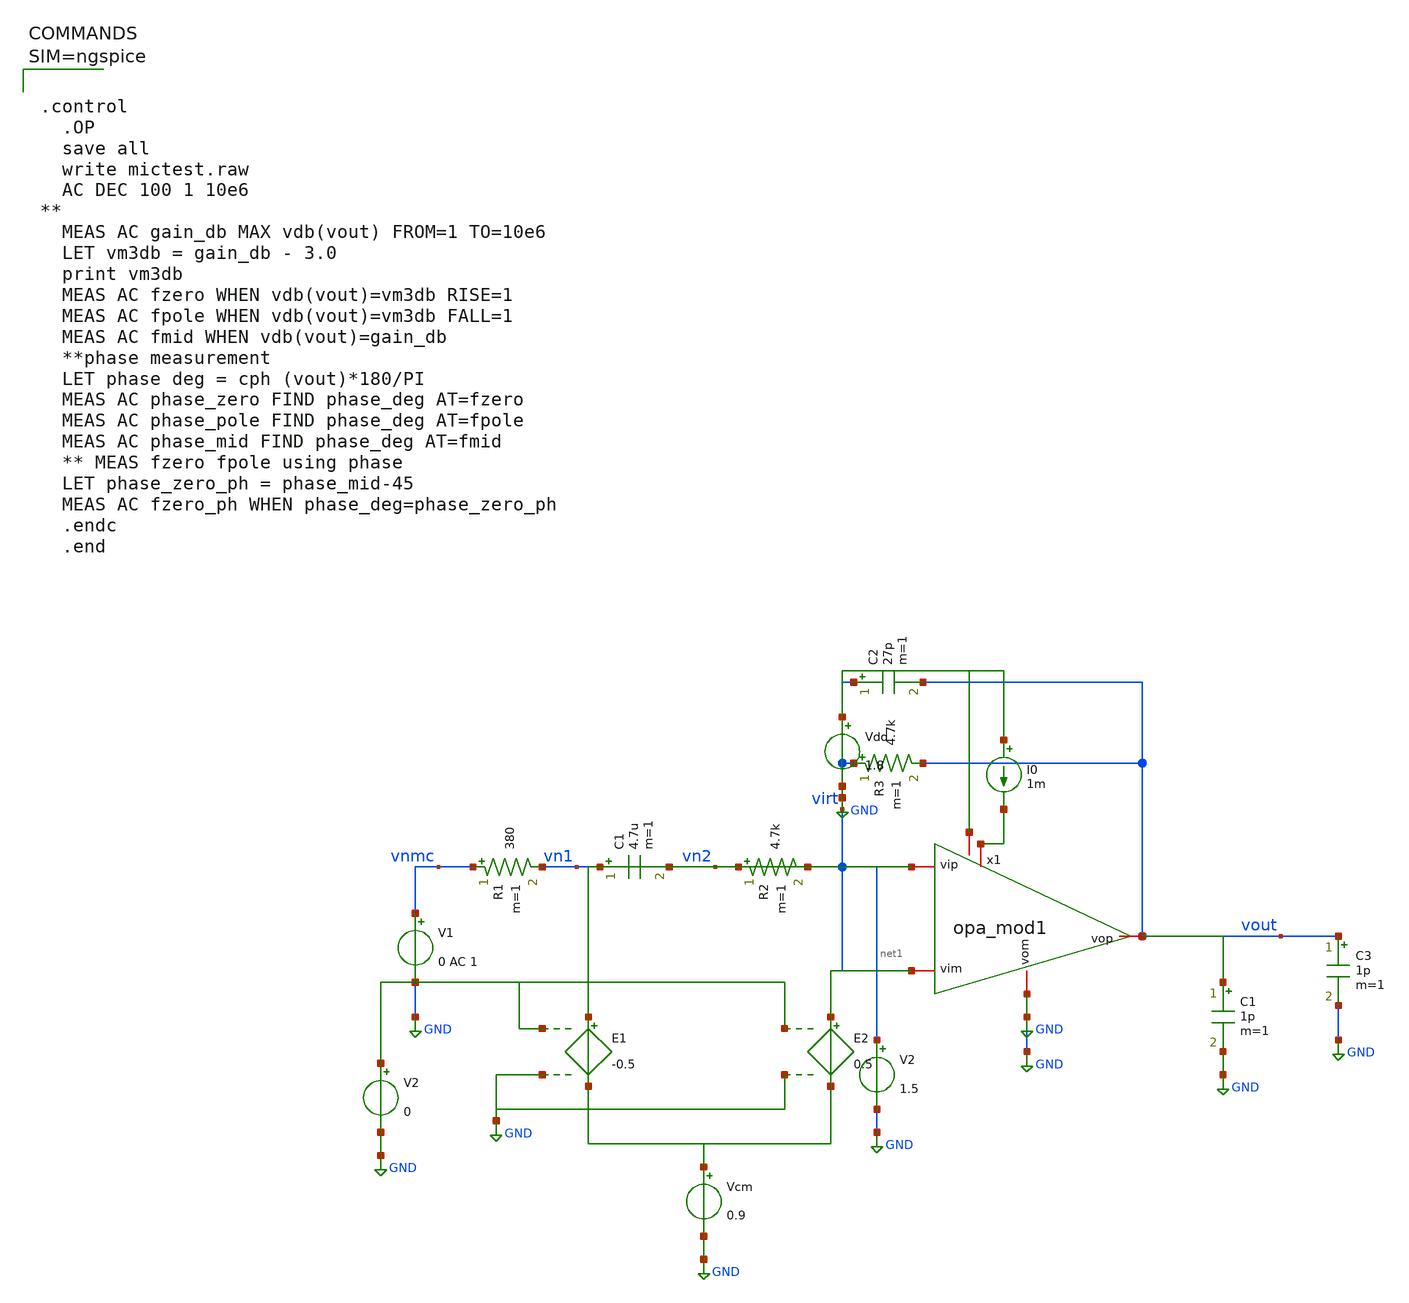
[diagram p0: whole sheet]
** sch_path: xschem/micTest_opamod1.sch
**.subckt micTest_opamod1
V1 vnmc GND 0 AC 1
C1 vn1 vn2 4.7u m=1
R1 vnmc vn1 380 m=1
R2 vn2 virt 4.7k m=1
R3 virt vout 4.7k m=1
C2 virt vout 27p m=1
V2 net1 GND 1.5
C3 vout GND 1p m=1
x1 vout net1 virt GND opa_mod1
**** begin user architecture code



.control
  .OP
  save all
  write mictest.raw
  AC DEC 100 1 10e6
**
  MEAS AC gain_db MAX vdb(vout) FROM=1 TO=10e6
  LET vm3db = gain_db - 3.0
  print vm3db
  MEAS AC fzero WHEN vdb(vout)=vm3db RISE=1
  MEAS AC fpole WHEN vdb(vout)=vm3db FALL=1
  MEAS AC fmid WHEN vdb(vout)=gain_db
  **phase measurement
  LET phase deg = cph (vout)*180/PI
  MEAS AC phase_zero FIND phase_deg AT=fzero
  MEAS AC phase_pole FIND phase_deg AT=fpole
  MEAS AC phase_mid FIND phase_deg AT=fmid
  ** MEAS fzero fpole using phase
  LET phase_zero_ph = phase_mid-45
  MEAS AC fzero_ph WHEN phase_deg=phase_zero_ph
  .endc
  .end




**** end user architecture code
**.ends

* expanding   symbol:  opa_mod1.sym # of pins=6
** sym_path: xschem/opa_mod1.sym
** sch_path: xschem/opa_mod1.sch
.subckt opa_mod1 vop vip vim vom
*.iopin vip
*.iopin vim
*.iopin vop
*.iopin vom
E1 vop vom vip vim 1000
.ends

.GLOBAL GND
.end
